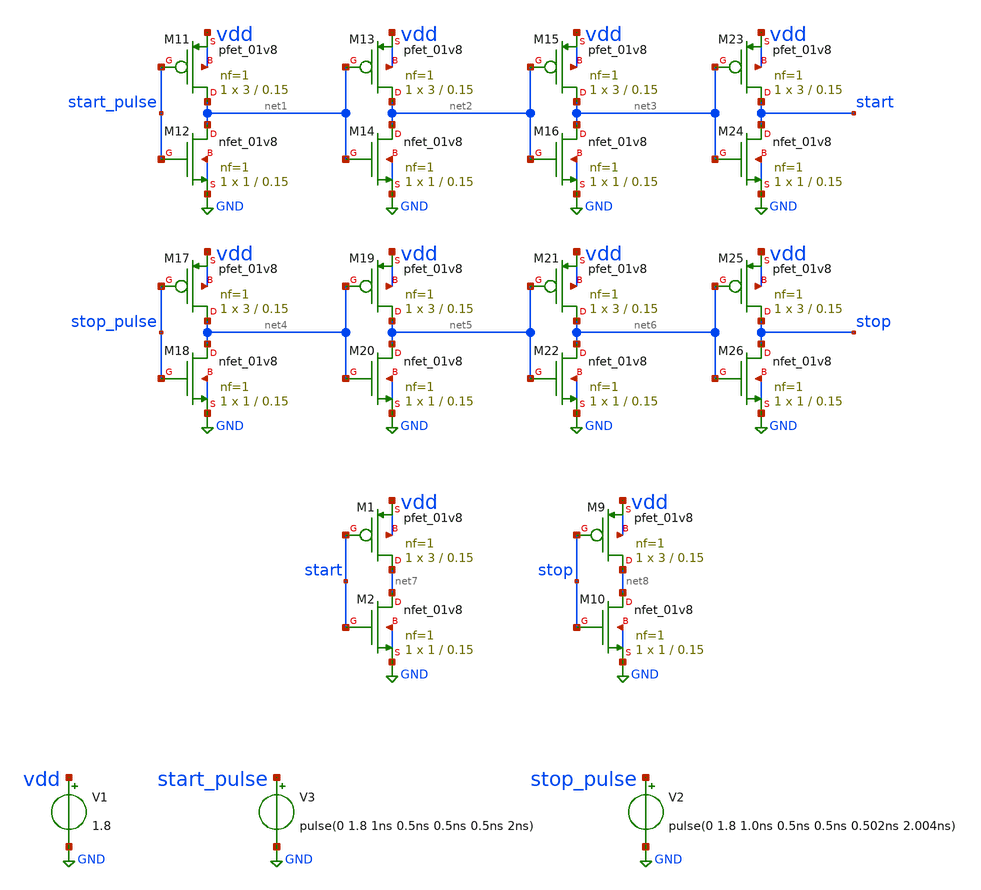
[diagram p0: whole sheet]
** sch_path: xschem/test_signals_tb.sch
**.subckt test_signals_tb
V2 stop_pulse GND pulse(0 1.8 1.0ns 0.5ns 0.5ns 0.502ns 2.004ns)
V3 start_pulse GND pulse(0 1.8 1ns 0.5ns 0.5ns 0.5ns 2ns)
XM11 net1 start_pulse vdd vdd sky130_fd_pr__pfet_01v8 L=0.15 W=3 nf=1 ad='int((nf+1)/2) * W/nf * 0.29'
+ as='int((nf+2)/2) * W/nf * 0.29' pd='2*int((nf+1)/2) * (W/nf + 0.29)' ps='2*int((nf+2)/2) * (W/nf + 0.29)'
+ nrd='0.29 / W' nrs='0.29 / W' sa=0 sb=0 sd=0 mult=1 m=1
XM12 net1 start_pulse GND GND sky130_fd_pr__nfet_01v8 L=0.15 W=1 nf=1 ad='int((nf+1)/2) * W/nf * 0.29'
+ as='int((nf+2)/2) * W/nf * 0.29' pd='2*int((nf+1)/2) * (W/nf + 0.29)' ps='2*int((nf+2)/2) * (W/nf + 0.29)'
+ nrd='0.29 / W' nrs='0.29 / W' sa=0 sb=0 sd=0 mult=1 m=1
XM13 net2 net1 vdd vdd sky130_fd_pr__pfet_01v8 L=0.15 W=3 nf=1 ad='int((nf+1)/2) * W/nf * 0.29' as='int((nf+2)/2) * W/nf * 0.29'
+ pd='2*int((nf+1)/2) * (W/nf + 0.29)' ps='2*int((nf+2)/2) * (W/nf + 0.29)' nrd='0.29 / W' nrs='0.29 / W'
+ sa=0 sb=0 sd=0 mult=1 m=1
XM14 net2 net1 GND GND sky130_fd_pr__nfet_01v8 L=0.15 W=1 nf=1 ad='int((nf+1)/2) * W/nf * 0.29' as='int((nf+2)/2) * W/nf * 0.29'
+ pd='2*int((nf+1)/2) * (W/nf + 0.29)' ps='2*int((nf+2)/2) * (W/nf + 0.29)' nrd='0.29 / W' nrs='0.29 / W'
+ sa=0 sb=0 sd=0 mult=1 m=1
XM15 net3 net2 vdd vdd sky130_fd_pr__pfet_01v8 L=0.15 W=3 nf=1 ad='int((nf+1)/2) * W/nf * 0.29' as='int((nf+2)/2) * W/nf * 0.29'
+ pd='2*int((nf+1)/2) * (W/nf + 0.29)' ps='2*int((nf+2)/2) * (W/nf + 0.29)' nrd='0.29 / W' nrs='0.29 / W'
+ sa=0 sb=0 sd=0 mult=1 m=1
XM16 net3 net2 GND GND sky130_fd_pr__nfet_01v8 L=0.15 W=1 nf=1 ad='int((nf+1)/2) * W/nf * 0.29' as='int((nf+2)/2) * W/nf * 0.29'
+ pd='2*int((nf+1)/2) * (W/nf + 0.29)' ps='2*int((nf+2)/2) * (W/nf + 0.29)' nrd='0.29 / W' nrs='0.29 / W'
+ sa=0 sb=0 sd=0 mult=1 m=1
XM17 net4 stop_pulse vdd vdd sky130_fd_pr__pfet_01v8 L=0.15 W=3 nf=1 ad='int((nf+1)/2) * W/nf * 0.29'
+ as='int((nf+2)/2) * W/nf * 0.29' pd='2*int((nf+1)/2) * (W/nf + 0.29)' ps='2*int((nf+2)/2) * (W/nf + 0.29)'
+ nrd='0.29 / W' nrs='0.29 / W' sa=0 sb=0 sd=0 mult=1 m=1
XM18 net4 stop_pulse GND GND sky130_fd_pr__nfet_01v8 L=0.15 W=1 nf=1 ad='int((nf+1)/2) * W/nf * 0.29'
+ as='int((nf+2)/2) * W/nf * 0.29' pd='2*int((nf+1)/2) * (W/nf + 0.29)' ps='2*int((nf+2)/2) * (W/nf + 0.29)'
+ nrd='0.29 / W' nrs='0.29 / W' sa=0 sb=0 sd=0 mult=1 m=1
XM19 net5 net4 vdd vdd sky130_fd_pr__pfet_01v8 L=0.15 W=3 nf=1 ad='int((nf+1)/2) * W/nf * 0.29' as='int((nf+2)/2) * W/nf * 0.29'
+ pd='2*int((nf+1)/2) * (W/nf + 0.29)' ps='2*int((nf+2)/2) * (W/nf + 0.29)' nrd='0.29 / W' nrs='0.29 / W'
+ sa=0 sb=0 sd=0 mult=1 m=1
XM20 net5 net4 GND GND sky130_fd_pr__nfet_01v8 L=0.15 W=1 nf=1 ad='int((nf+1)/2) * W/nf * 0.29' as='int((nf+2)/2) * W/nf * 0.29'
+ pd='2*int((nf+1)/2) * (W/nf + 0.29)' ps='2*int((nf+2)/2) * (W/nf + 0.29)' nrd='0.29 / W' nrs='0.29 / W'
+ sa=0 sb=0 sd=0 mult=1 m=1
XM21 net6 net5 vdd vdd sky130_fd_pr__pfet_01v8 L=0.15 W=3 nf=1 ad='int((nf+1)/2) * W/nf * 0.29' as='int((nf+2)/2) * W/nf * 0.29'
+ pd='2*int((nf+1)/2) * (W/nf + 0.29)' ps='2*int((nf+2)/2) * (W/nf + 0.29)' nrd='0.29 / W' nrs='0.29 / W'
+ sa=0 sb=0 sd=0 mult=1 m=1
XM22 net6 net5 GND GND sky130_fd_pr__nfet_01v8 L=0.15 W=1 nf=1 ad='int((nf+1)/2) * W/nf * 0.29' as='int((nf+2)/2) * W/nf * 0.29'
+ pd='2*int((nf+1)/2) * (W/nf + 0.29)' ps='2*int((nf+2)/2) * (W/nf + 0.29)' nrd='0.29 / W' nrs='0.29 / W'
+ sa=0 sb=0 sd=0 mult=1 m=1
XM23 start net3 vdd vdd sky130_fd_pr__pfet_01v8 L=0.15 W=3 nf=1 ad='int((nf+1)/2) * W/nf * 0.29' as='int((nf+2)/2) * W/nf * 0.29'
+ pd='2*int((nf+1)/2) * (W/nf + 0.29)' ps='2*int((nf+2)/2) * (W/nf + 0.29)' nrd='0.29 / W' nrs='0.29 / W'
+ sa=0 sb=0 sd=0 mult=1 m=1
XM24 start net3 GND GND sky130_fd_pr__nfet_01v8 L=0.15 W=1 nf=1 ad='int((nf+1)/2) * W/nf * 0.29' as='int((nf+2)/2) * W/nf * 0.29'
+ pd='2*int((nf+1)/2) * (W/nf + 0.29)' ps='2*int((nf+2)/2) * (W/nf + 0.29)' nrd='0.29 / W' nrs='0.29 / W'
+ sa=0 sb=0 sd=0 mult=1 m=1
XM25 stop net6 vdd vdd sky130_fd_pr__pfet_01v8 L=0.15 W=3 nf=1 ad='int((nf+1)/2) * W/nf * 0.29' as='int((nf+2)/2) * W/nf * 0.29'
+ pd='2*int((nf+1)/2) * (W/nf + 0.29)' ps='2*int((nf+2)/2) * (W/nf + 0.29)' nrd='0.29 / W' nrs='0.29 / W'
+ sa=0 sb=0 sd=0 mult=1 m=1
XM26 stop net6 GND GND sky130_fd_pr__nfet_01v8 L=0.15 W=1 nf=1 ad='int((nf+1)/2) * W/nf * 0.29' as='int((nf+2)/2) * W/nf * 0.29'
+ pd='2*int((nf+1)/2) * (W/nf + 0.29)' ps='2*int((nf+2)/2) * (W/nf + 0.29)' nrd='0.29 / W' nrs='0.29 / W'
+ sa=0 sb=0 sd=0 mult=1 m=1
XM1 net7 start vdd vdd sky130_fd_pr__pfet_01v8 L=0.15 W=3 nf=1 ad='int((nf+1)/2) * W/nf * 0.29' as='int((nf+2)/2) * W/nf * 0.29'
+ pd='2*int((nf+1)/2) * (W/nf + 0.29)' ps='2*int((nf+2)/2) * (W/nf + 0.29)' nrd='0.29 / W' nrs='0.29 / W'
+ sa=0 sb=0 sd=0 mult=1 m=1
XM2 net7 start GND GND sky130_fd_pr__nfet_01v8 L=0.15 W=1 nf=1 ad='int((nf+1)/2) * W/nf * 0.29' as='int((nf+2)/2) * W/nf * 0.29'
+ pd='2*int((nf+1)/2) * (W/nf + 0.29)' ps='2*int((nf+2)/2) * (W/nf + 0.29)' nrd='0.29 / W' nrs='0.29 / W'
+ sa=0 sb=0 sd=0 mult=1 m=1
XM9 net8 stop vdd vdd sky130_fd_pr__pfet_01v8 L=0.15 W=3 nf=1 ad='int((nf+1)/2) * W/nf * 0.29' as='int((nf+2)/2) * W/nf * 0.29'
+ pd='2*int((nf+1)/2) * (W/nf + 0.29)' ps='2*int((nf+2)/2) * (W/nf + 0.29)' nrd='0.29 / W' nrs='0.29 / W'
+ sa=0 sb=0 sd=0 mult=1 m=1
XM10 net8 stop GND GND sky130_fd_pr__nfet_01v8 L=0.15 W=1 nf=1 ad='int((nf+1)/2) * W/nf * 0.29' as='int((nf+2)/2) * W/nf * 0.29'
+ pd='2*int((nf+1)/2) * (W/nf + 0.29)' ps='2*int((nf+2)/2) * (W/nf + 0.29)' nrd='0.29 / W' nrs='0.29 / W'
+ sa=0 sb=0 sd=0 mult=1 m=1
V1 vdd GND 1.8
**** begin user architecture code

** opencircuitdesign pdks install
.lib $::SKYWATER_MODELS/sky130.lib.spice tt





.tran 0.001n 320n
.save v(start) v(stop)

.control
run
set wr_vecnames
wrdata tdc_test_signals_tb.txt v(start) v(stop)
.endc


**** end user architecture code
**.ends
.GLOBAL GND
.end
